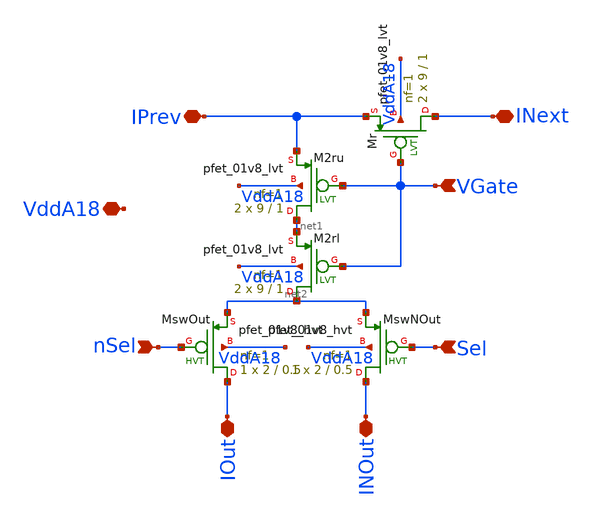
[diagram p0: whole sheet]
** sch_path: analog/xschem/BiasDividerFineCell.sch
**.subckt BiasDividerFineCell INext IOut IPrev VGate VddA18 nSel Sel INOut
*.iopin INext
*.iopin IOut
*.iopin IPrev
*.ipin VGate
*.iopin VddA18
*.ipin nSel
*.ipin Sel
*.iopin INOut
XMr INext VGate IPrev VddA18 sky130_fd_pr__pfet_01v8_lvt L=1 W=9 nf=1 ad='int((1 + 1)/2) * 9 / 1 * 0.29'
+ as='int((1 + 2)/2) * 9 / 1 * 0.29' pd='2*int((1 + 1)/2) * (9 / 1 + 0.29)' ps='2*int((1 + 2)/2) * (9 / 1 + 0.29)'
+ nrd='0.29 / 9 ' nrs='0.29 / 9 ' sa=0 sb=0 sd=0 mult=2 m=2
XM2ru net1 VGate IPrev VddA18 sky130_fd_pr__pfet_01v8_lvt L=1 W=9 nf=1 ad='int((1 + 1)/2) * 9 / 1 * 0.29'
+ as='int((1 + 2)/2) * 9 / 1 * 0.29' pd='2*int((1 + 1)/2) * (9 / 1 + 0.29)' ps='2*int((1 + 2)/2) * (9 / 1 + 0.29)'
+ nrd='0.29 / 9 ' nrs='0.29 / 9 ' sa=0 sb=0 sd=0 mult=2 m=2
XM2rl net2 VGate net1 VddA18 sky130_fd_pr__pfet_01v8_lvt L=1 W=9 nf=1 ad='int((1 + 1)/2) * 9 / 1 * 0.29'
+ as='int((1 + 2)/2) * 9 / 1 * 0.29' pd='2*int((1 + 1)/2) * (9 / 1 + 0.29)' ps='2*int((1 + 2)/2) * (9 / 1 + 0.29)'
+ nrd='0.29 / 9 ' nrs='0.29 / 9 ' sa=0 sb=0 sd=0 mult=2 m=2
XMswNOut INOut Sel net2 VddA18 sky130_fd_pr__pfet_01v8_hvt L=0.5 W=2 nf=1 ad='int((1 + 1)/2) * 2 / 1 * 0.29'
+ as='int((1 + 2)/2) * 2 / 1 * 0.29' pd='2*int((1 + 1)/2) * (2 / 1 + 0.29)' ps='2*int((1 + 2)/2) * (2 / 1 + 0.29)'
+ nrd='0.29 / 2 ' nrs='0.29 / 2 ' sa=0 sb=0 sd=0 mult=1 m=1
XMswOut IOut nSel net2 VddA18 sky130_fd_pr__pfet_01v8_hvt L=0.5 W=2 nf=1 ad='int((1 + 1)/2) * 2 / 1 * 0.29'
+ as='int((1 + 2)/2) * 2 / 1 * 0.29' pd='2*int((1 + 1)/2) * (2 / 1 + 0.29)' ps='2*int((1 + 2)/2) * (2 / 1 + 0.29)'
+ nrd='0.29 / 2 ' nrs='0.29 / 2 ' sa=0 sb=0 sd=0 mult=1 m=1
**.ends
.end
